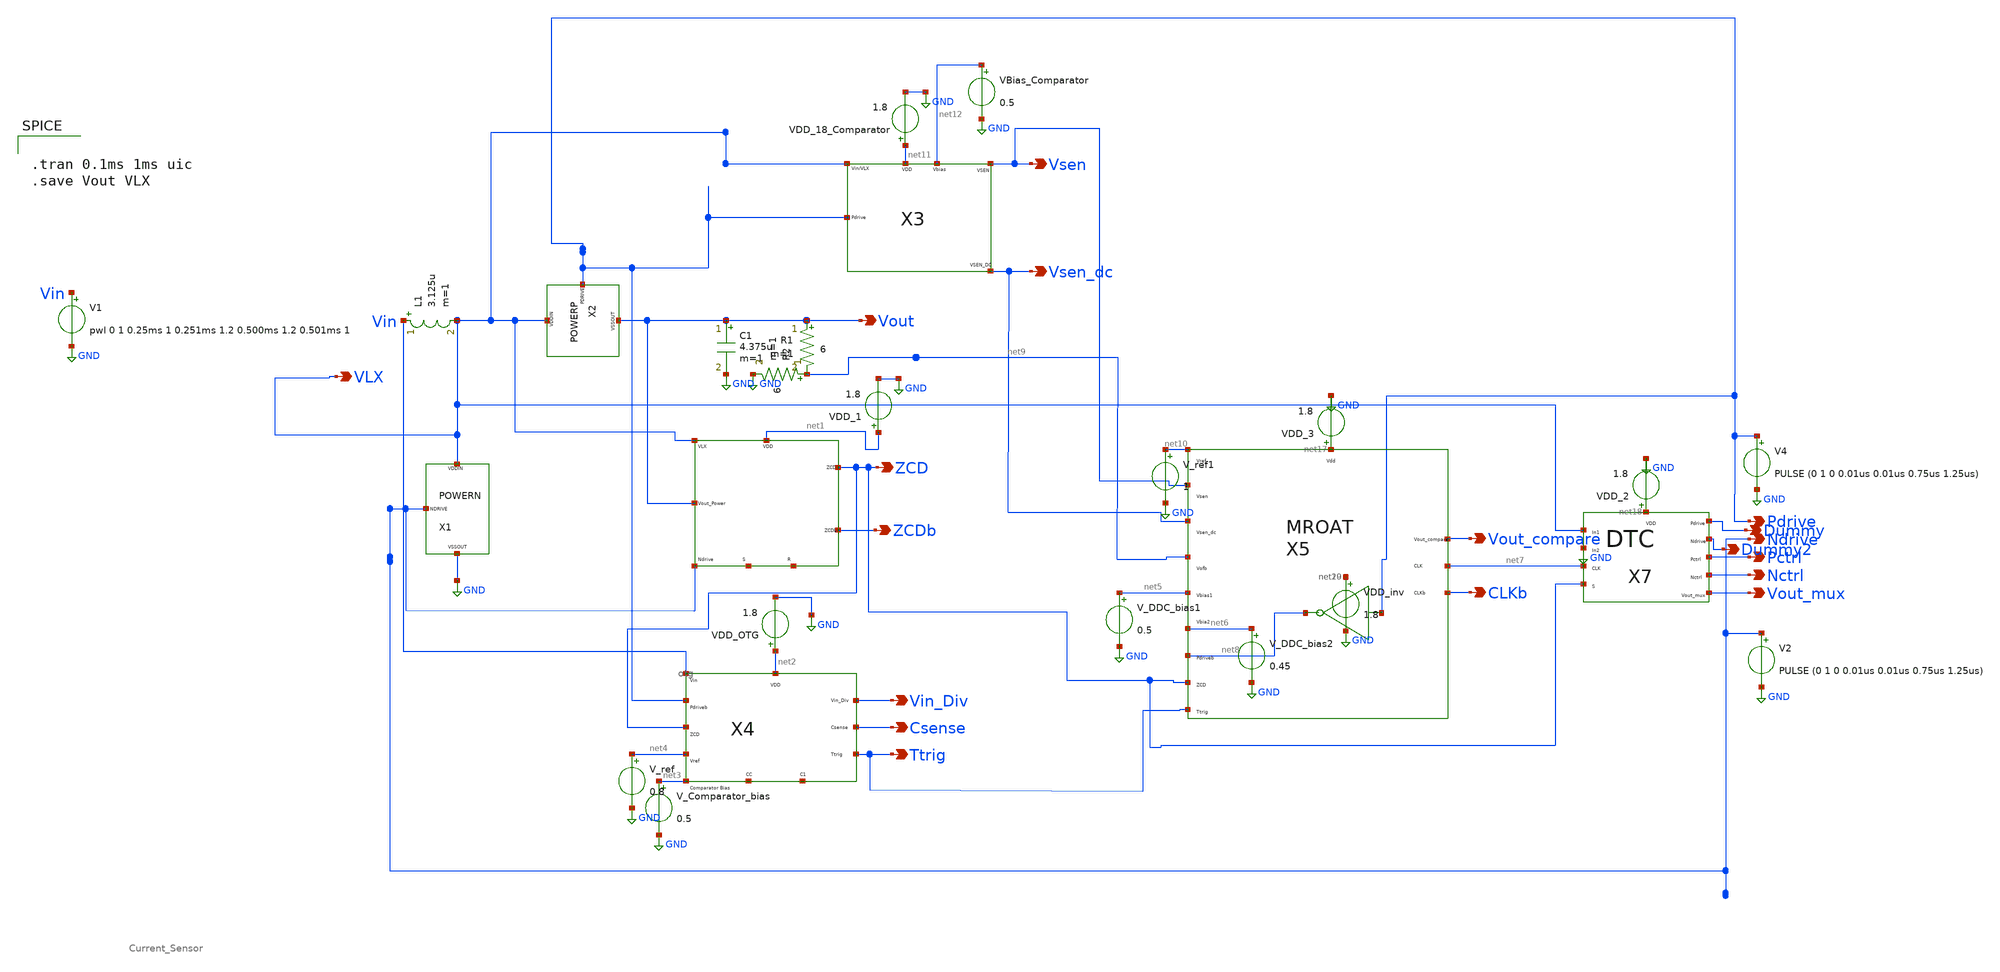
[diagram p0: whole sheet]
** sch_path: Spice_Files/Basic_Boost.sch
**.subckt Basic_Boost Vout Vsen Vsen_dc ZCD ZCDb Vin_Div Csense Ttrig Pctrl Nctrl Vout_mux Ndrive
*+ Pdrive CLKb Vout_compare Dummy Dummy2 VLX
*.opin Vout
*.opin Vsen
*.opin Vsen_dc
*.opin ZCD
*.opin ZCDb
*.opin Vin_Div
*.opin Csense
*.opin Ttrig
*.opin Pctrl
*.opin Nctrl
*.opin Vout_mux
*.opin Ndrive
*.opin Pdrive
*.opin CLKb
*.opin Vout_compare
*.opin Dummy
*.opin Dummy2
*.opin VLX
C1 Vout GND 4.375u m=1
R1 Vout net9 6 m=1
L1 Vin VLX 3.125u m=1
V1 Vin GND pwl 0 1 0.25ms 1 0.251ms 1.2 0.500ms 1.2 0.501ms 1
X1 Ndrive VLX GND powern
X2 Pdrive VLX Vout powerp
VDD_18_Comparator net11 GND 1.8
VBias_Comparator net12 GND 0.5
X3 Vsen Vsen_dc Pdrive VLX net11 net12 Current_Sensor
X1 VLX Vout Ndrive net1 ZCD ZCDb net13 net14 zcd
VDD_1 net1 GND 1.8
X4 Vin Pdrive ZCD net4 net3 net2 Vin_Div Csense Ttrig net15 net16 otg
VDD_OTG net2 GND 1.8
V_Comparator_bias net3 GND 0.5
V_ref net4 GND 0.8
X5 net10 Vsen Vsen_dc net9 net5 net6 net17 Vout_compare net8 ZCD Ttrig net7 CLKb mroat
V_DDC_bias1 net5 GND 0.5
V_DDC_bias2 net6 GND 0.45
X7 net18 VLX GND net7 ZCD Dummy Dummy2 Pctrl Nctrl Vout_mux dtc
VDD_2 net18 GND 1.8
VDD_3 net17 GND 1.8
VDD_inv net19 GND 1.8
R2 net9 GND 6 m=1
V_ref1 net10 GND 1
V4 Pdrive GND PULSE (0 1 0 0.01us 0.01us 0.75us 1.25us)
V2 Ndrive GND PULSE (0 1 0 0.01us 0.01us 0.75us 1.25us)
**** begin user architecture code


.tran 0.1ms 1ms uic
.save Vout VLX


** opencircuitdesign pdks install
.lib $::SKYWATER_MODELS/sky130.lib.spice tt_mm


**** end user architecture code
**.ends
.GLOBAL GND
.end
